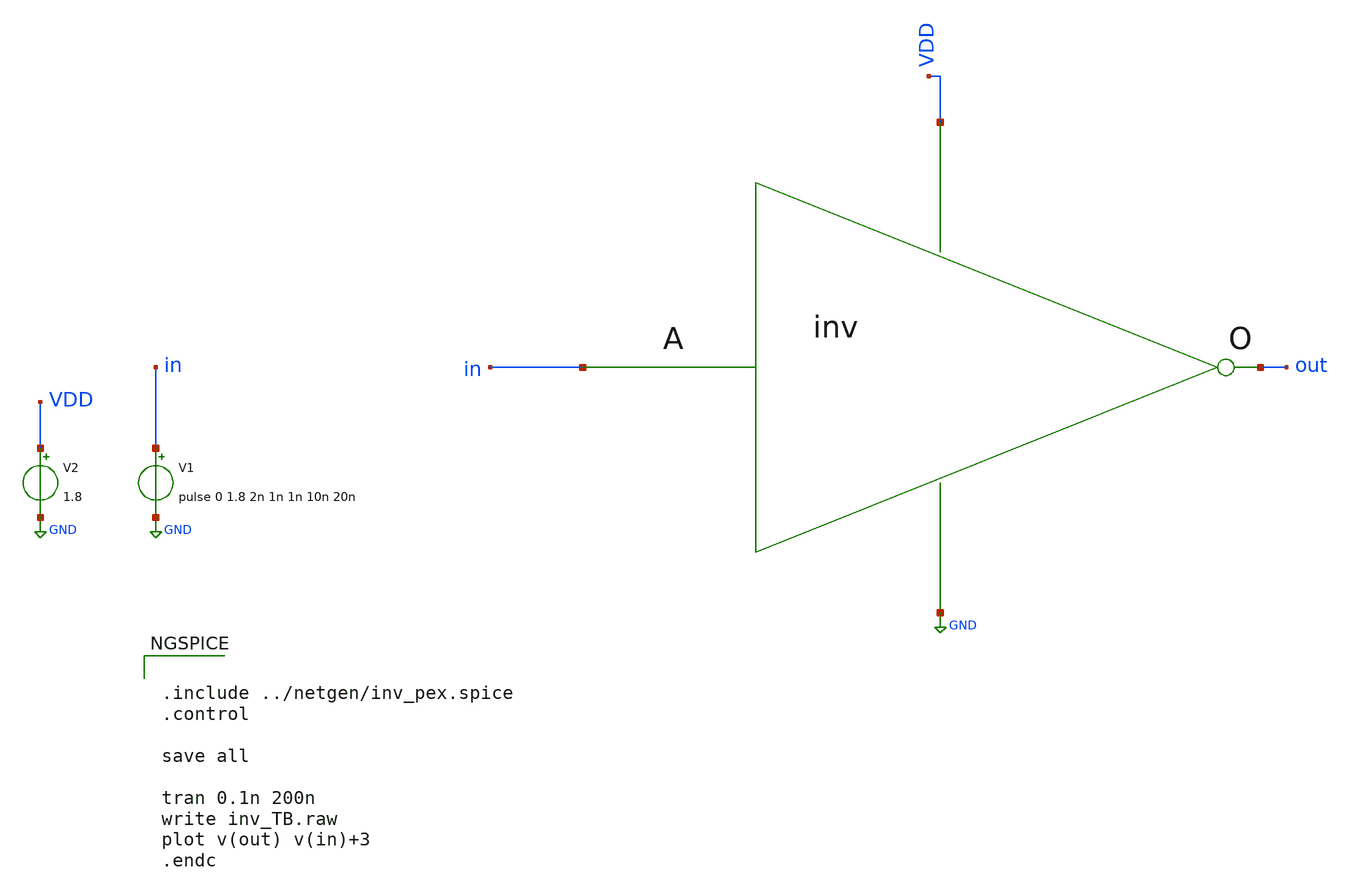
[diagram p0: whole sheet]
** sch_path: inv_TB.sch
**.subckt inv_TB
X1 in VDD out GND inv
V1 in GND pulse 0 1.8 2n 1n 1n 10n 20n
V2 VDD GND 1.8
**** begin user architecture code

** opencircuitdesign pdks install
.lib $::SKYWATER_MODELS/sky130.lib.spice tt_mm




.include ../netgen/inv_pex.spice
.control

save all

tran 0.1n 200n
write inv_TB.raw
plot v(out) v(in)+3
.endc


**** end user architecture code
**.ends
.GLOBAL GND
.end
